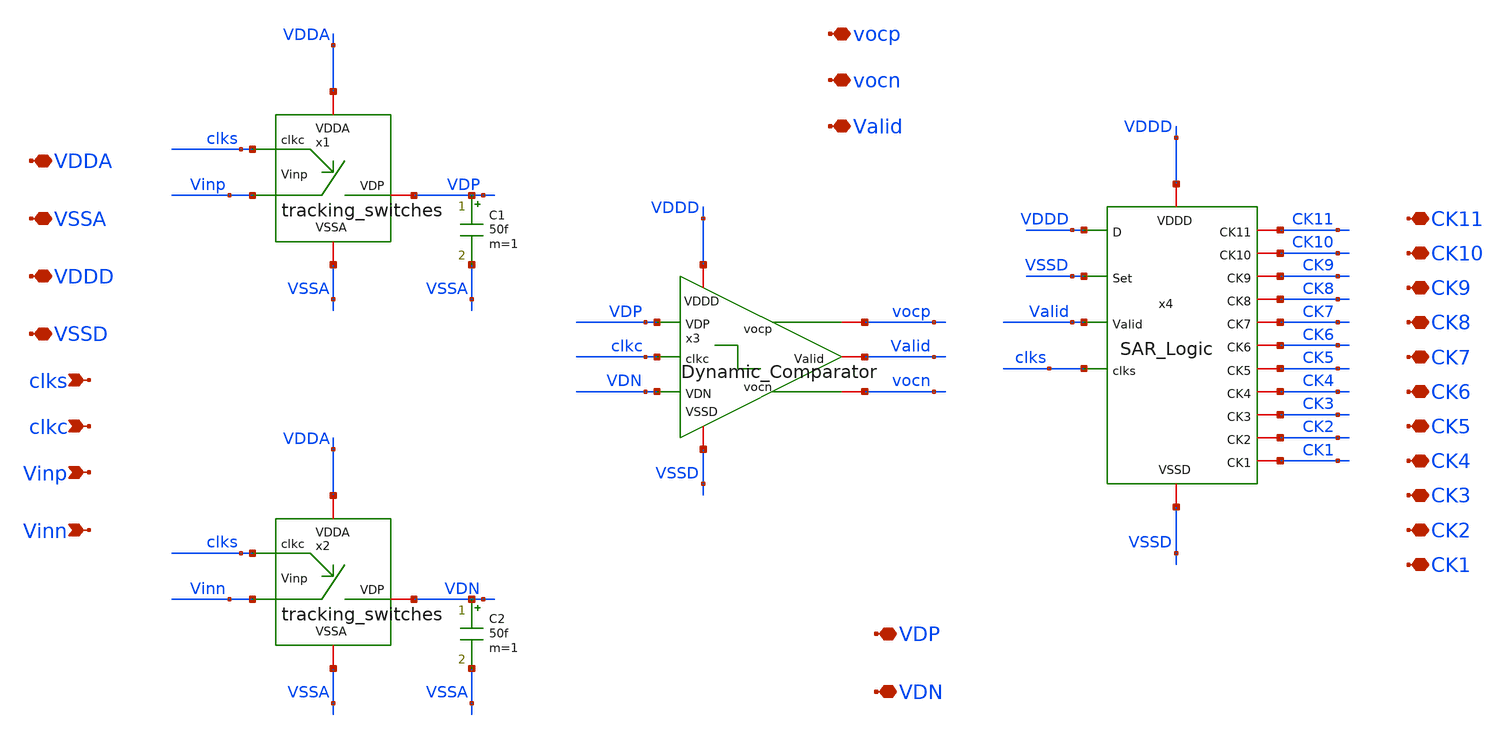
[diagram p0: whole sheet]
** sch_path: SAR_ADC/integration/TrackingSW_DynComp_SARLogic.sch
**.subckt TrackingSW_DynComp_SARLogic VDDD VSSD clks VDDA VSSA clkc Vinp Vinn VDP VDN CK11 CK10 CK9
*+ CK8 CK7 CK6 CK5 CK4 CK3 CK2 CK1 vocp vocn Valid
*.iopin VDDD
*.iopin VSSD
*.ipin clks
*.iopin VDDA
*.iopin VSSA
*.ipin clkc
*.ipin Vinp
*.ipin Vinn
*.iopin VDP
*.iopin VDN
*.iopin CK11
*.iopin CK10
*.iopin CK9
*.iopin CK8
*.iopin CK7
*.iopin CK6
*.iopin CK5
*.iopin CK4
*.iopin CK3
*.iopin CK2
*.iopin CK1
*.iopin vocp
*.iopin vocn
*.iopin Valid
x1 VDP VDDA VSSA clks Vinp tracking_switches
x2 VDN VDDA VSSA clks Vinn tracking_switches
x3 vocp vocn VDDD VSSD VDP VDN Valid clkc Dynamic_Comparator
x4 CK11 VDDD CK1 CK6 VSSD CK10 CK5 CK9 CK4 clks CK8 CK3 Valid CK2 CK7 VSSD VDDD SAR_Logic
C1 VDP VSSA 50f m=1
C2 VDN VSSA 50f m=1
**.ends
.end
